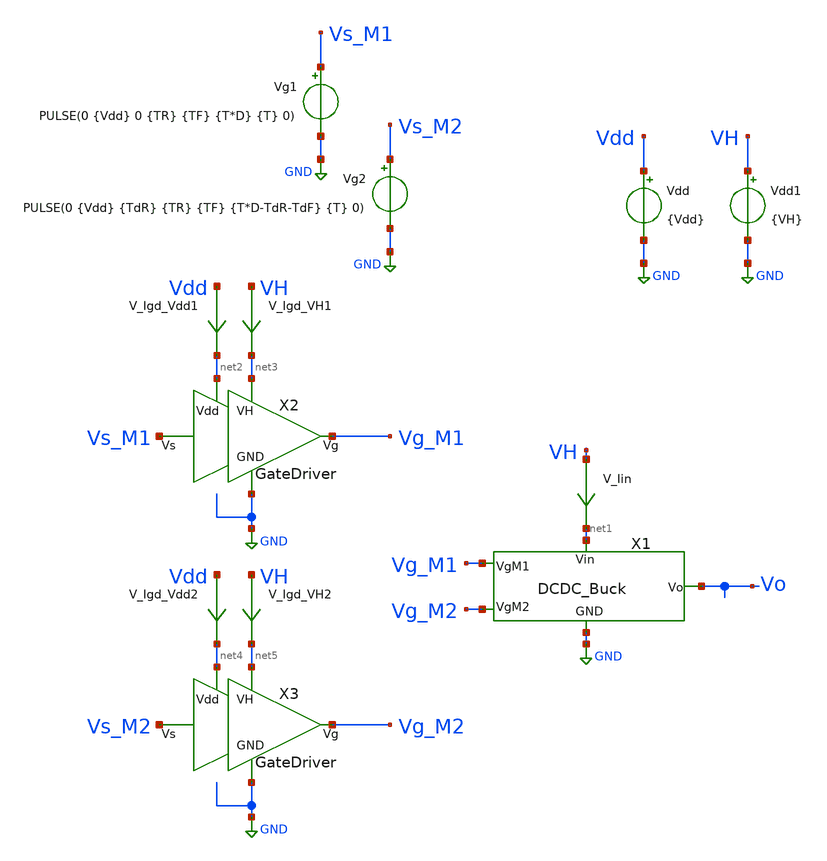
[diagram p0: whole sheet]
** sch_path: ChipUSM_AnalogTrack24/GD/TB_DCDCBuck+GateDrivers.sch
**.subckt TB_DCDCBuck+GateDrivers
Vdd Vdd GND {Vdd}
Vg2 Vs_M2 GND PULSE(0 {Vdd} {TdR} {TR} {TF} {T*D-TdR-TdF} {T} 0)
Vg1 Vs_M1 GND PULSE(0 {Vdd} 0 {TR} {TF} {T*D} {T} 0)
V_Iin VH net1 0
.save i(v_iin)
Vdd1 VH GND {VH}
V_Igd_VH1 VH net3 0
.save i(v_igd_vh1)
V_Igd_VH2 VH net5 0
.save i(v_igd_vh2)
V_Igd_Vdd2 Vdd net4 0
.save i(v_igd_vdd2)
V_Igd_Vdd1 Vdd net2 0
.save i(v_igd_vdd1)
X1 Vg_M1 Vg_M2 GND net1 Vo DCDC_Buck
X3 Vs_M2 Vg_M2 net4 net5 GND GateDriver
X2 Vs_M1 Vg_M1 net2 net3 GND GateDriver
**** begin user architecture code

.lib cornerMOShv.lib mos_tt
.lib cornerMOSlv.lib mos_tt
*.lib cornerMOShv.lib mos_ff
*.lib cornerMOSlv.lib mos_ff
*.lib cornerMOShv.lib mos_ss
*.lib cornerMOSlv.lib mos_ss
*.lib cornerMOShv.lib mos_sf
*.lib cornerMOSlv.lib mos_sf
*.lib cornerMOShv.lib mos_fs
*.lib cornerMOSlv.lib mos_fs



.param Vdd = 1.2
.param VH = 3.3
.param Del = 0

.param D = 0.615

* fs = 10MHz
.param T = 0.1u

.param TR = 1n
.param TF = 1n
.param TdR = 1n
.param TdF = 1n

.option temp = 27
*.option temp = 125
*.option temp = -40





*Parametros
*Filtro

* Io=1A 10MHz
.param L = 275n
.param R = 1.2
.param C = 31.25n

* Io=1A 8.4MHz
*.param L = 327n
*.param R = 1.2
*.param C = 37n

* Io=100mA 8.4MHz
*.param L = 3.27u
*.param R = 12
*.param C = 3.7n

* Io=100mA y 1A @8.4MHz
*.param L = 595n
*.param R = 12
*.param R = 1.2
*.param R = 0.4
*.param R = 0.6
*.param R = 0.3
*.param C = 20.5n

* Io =1A 1MHz
*.param L = 2.75u
*.param R = 1.2
*.param C = 312.5n

* Io =100mA 1MHz
*.param L = 27.5u
*.param R = 12
*.param C = 31.25n

* Io =100mA y 1A @1MHz
*.param L = 5u
*.param R = 12
*.param R = 1.2
*.param C = 171n







.option method=gear

.save all  @n.x1.xm1.nsg13_hv_pmos[ids]  @n.x1.xm2.nsg13_hv_nmos[ids]
.param SimTime = 5u
.param T1=2.381u
.control
reset
set color0 = white
tran 1n 5u
let Io = i(v.x1.V_Io)
let Id_M1 = @n.x1.xm1.nsg13_hv_pmos[ids]
let Id_M2 = @n.x1.xm2.nsg13_hv_nmos[ids]
let Po = Io*v(Vo)
let I_in = i(V_Iin)
let Pin = I_in*v(VH)
let Vsd_M1 = v(VH) - v(x1.Vc)
let Vds_M2 = v(x1.Vc)
let P_M1 = Vsd_M1*Id_M1
let P_M2 = -Vds_M2*Id_M2
let P_GD_Vdd = v(Vdd)*(i(V_Igd_Vdd1)+i(V_Igd_Vdd2))
let P_GD_VH = v(VH)*(i(V_Igd_VH1)+i(V_Igd_VH2))
let DataMeasBegin = SimTime-1u

meas tran Vo_mean AVG v(Vo) from=2u to=4u
meas tran Io_mean AVG Io from=2u to=4u
meas tran Po_mean AVG Po from=2u to=4u
meas tran Pin_mean AVG Pin from=2u to=4u
meas tran P_M1_mean AVG P_M1 from=2u to=4u
meas tran P_M2_mean AVG P_M2 from=2u to=4u
meas tran P_GD_Vdd_mean AVG P_GD_Vdd from=2u to=4u
meas tran P_GD_VH_mean AVG P_GD_VH from=2u to=4u

meas TRAN tdR TRIG v(Vg_M1) VAL=0.33 RISE=1 TARG v(Vg_M2) VAL=0.33 RISE=1
meas TRAN tdF TRIG v(Vg_M1) VAL=2.97 FALL=1 TARG v(Vg_M2) VAL=2.97 FALL=1

let P_GD = P_GD_Vdd_mean+P_GD_VH_mean
let Pin_tot_mean = P_GD + Pin_mean
let eff = 100*Po_mean/Pin_tot_mean
let eff_DCDC = 100*Po_mean/Pin_mean
let loss_M1 = 100*P_M1_mean/Pin_tot_mean
let loss_M2 = 100*P_M2_mean/Pin_tot_mean
let loss_GD = 100*P_GD/Pin_tot_mean
let sumaPot = eff+loss_M1+loss_M2+loss_GD
print Pin_tot_mean eff eff_DCDC loss_M1 loss_M2 loss_GD sumaPot

plot Io i(v.x1.V_IL)
plot Id_M1 Id_M2
plot v(Vo)
plot Po Pin
*plot P_M1 P_M2
plot v(x1.Vc)
plot v(Vg_M1) v(Vg_M2)
.endc



.end




*M1 hvPMOS
.param temp=27
.param mult_M1 = 1
.param w_M1 =10u
.param l_M1 = 0.4u
.param ng_M1 = 1

*M2 hvNMOS
.param mult_M2 = 1
.param w_M2 =10u
.param l_M2 =0.45u
.param ng_M2 =1








.param temp=27

.param mult_13 = 1
.param mult_24 = 1
.param mult_5 = 1
.param mult_6 = 1
.param mult_7 = 1
.param mult_8 = 1
.param mult_9 = 1
.param mult_10 = 1


.param ng_13 = 1
.param ng_24 = 1
.param ng_5 = 1
.param ng_6 = 1
.param ng_7 = 1
.param ng_8 = 1
.param ng_9 = 1
.param ng_10 = 1

.param l_1357 = 0.45u
.param w_1357 = 0.3u
.param l_2468 = 0.4u
.param w_2468 = 0.3u
.param l_9 = 0.13u
.param w_9 = 0.15u
.param l_10 = 0.13u
.param w_10 = 0.15u







**** end user architecture code
**.ends

* expanding   symbol:
*+  /home/designer/shared/simulations/IHP-sg13g2/Simulaciones/Campamento-ChipUSM-2024/ChipUSM_AnalogTrack24/DCDCBuck/DCDC_Buck.sym # of pins=5
** sym_path: /home/designer/shared/simulations/IHP-sg13g2/Simulaciones/Campamento-ChipUSM-2024/ChipUSM_AnalogTrack24/DCDCBuck/DCDC_Buck.sym
** sch_path: /home/designer/shared/simulations/IHP-sg13g2/Simulaciones/Campamento-ChipUSM-2024/ChipUSM_AnalogTrack24/DCDCBuck/DCDC_Buck.sch
.subckt DCDC_Buck VgM1 VgM2 GND Vin Vo
*.iopin Vin
*.ipin VgM1
*.ipin VgM2
*.iopin Vo
*.iopin GND
L1 net2 net1 {L} m=1
C1 net1 GND {C} m=1
V_Io net1 Vo 0
.save i(v_io)
V_IL Vc net2 0
.save i(v_il)
R1 Vo GND {R} m=1
V_IM2 Vc net3 0
.save i(v_im2)
XM3 Vc VgM1 Vin Vin sg13_hv_pmos w={w_M1} l={l_M1} ng={ng_M1} m={mult_M1} mm_ok=1
XM1 GND VgM2 net3 GND sg13_hv_nmos w={w_M2} l={l_M2} ng={ng_M2} m={mult_M2} mm_ok=1
.ends


* expanding   symbol:
*+  /home/designer/shared/simulations/IHP-sg13g2/Simulaciones/Campamento-ChipUSM-2024/ChipUSM_AnalogTrack24/GD/GateDriver.sym # of pins=5
** sym_path: ChipUSM_AnalogTrack24/GD/GateDriver.sym
** sch_path: ChipUSM_AnalogTrack24/GD/GateDriver.sch
.subckt GateDriver Vs Vg Vdd VH GND
*.iopin VH
*.iopin Vdd
*.ipin Vs
*.opin Vg
*.iopin GND
XMD9 VgMD2 Vs Vdd Vdd sg13_lv_pmos w={w_9} l={l_9} ng={ng_9} m={mult_9} mm_ok=1
XMD10 GND Vs VgMD2 GND sg13_lv_nmos w={w_10} l={l_10} ng={ng_10} m={mult_10} mm_ok=1
XMD1 VgMD5 net1 VH VH sg13_hv_pmos w={w_1357} l={l_1357} ng={ng_13} m={mult_13} mm_ok=1
XMD3 net1 VgMD5 VH VH sg13_hv_pmos w={w_1357} l={l_1357} ng={ng_13} m={mult_13} mm_ok=1
XMD5 net2 VgMD5 VH VH sg13_hv_pmos w={w_1357} l={l_1357} ng={ng_5} m={mult_5} mm_ok=1
XMD7 Vg VgMd78 VH VH sg13_hv_pmos w={w_1357} l={l_1357} ng={ng_7} m={mult_7} mm_ok=1
XMD2 GND VgMD2 VgMD5 GND sg13_hv_nmos w={w_2468} l={l_2468} ng={ng_24} m={mult_24} mm_ok=1
XMD4 GND Vs net1 GND sg13_hv_nmos w={w_2468} l={l_2468} ng={ng_24} m={mult_24} mm_ok=1
XMD6 GND Vs net2 GND sg13_hv_nmos w={w_2468} l={l_2468} ng={ng_6} m={mult_6} mm_ok=1
XMD8 GND VgMd78 Vg GND sg13_hv_nmos w={w_2468} l={l_2468} ng={ng_8} m={mult_8} mm_ok=1
VIg78 net2 VgMd78 0
.save i(vig78)
.ends

.GLOBAL GND
.end
